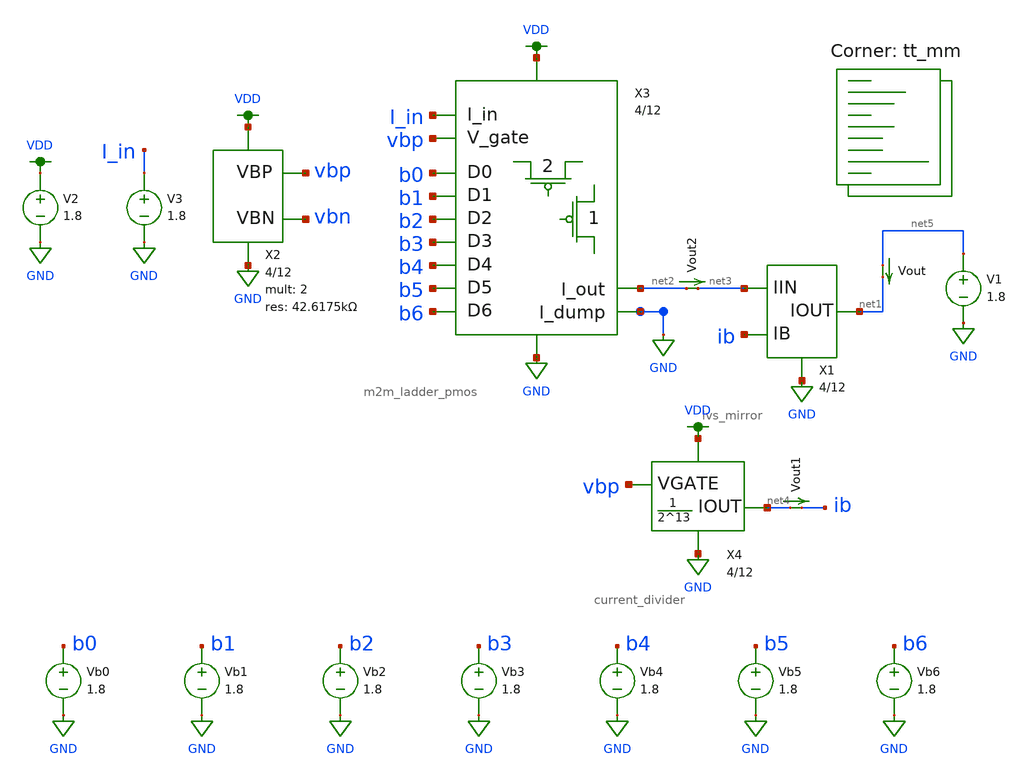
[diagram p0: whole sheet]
** sch_path: dac/schematic/m2m_ladder_biased_mirrored_mm_tb.sch
**.subckt m2m_ladder_biased_mirrored_mm_tb
Vb0 b0 GND 1.8
Vb1 b1 GND 1.8
Vb2 b2 GND 1.8
Vb3 b3 GND 1.8
Vb4 b4 GND 1.8
Vb5 b5 GND 1.8
Vb6 b6 GND 1.8
V2 VDD GND 1.8
X2 vbp VDD GND vbn bias_gen u_w=4 u_l=12 m=2 r=42.6175k
V3 I_in GND 1.8
X3 VDD GND b0 b1 b2 b3 b4 b5 b6 vbp I_in GND net2 m2m_ladder_pmos u_w=4 u_l=12
Vout2 net2 net3 0
.save i(vout2)
X1 GND net3 ib net1 lvs_mirror u_w=4 u_l=12 m=2 r=1M
Vout net5 net1 0
.save i(vout)
V1 net5 GND 1.8
X4 GND VDD net4 vbp current_divider u_w=4 u_l=12
Vout1 net4 ib 0
.save i(vout1)
**** begin user architecture code


.control
  set wr_vecnames
  set wr_singlescale
  let code = 0
  while code < 128
    if code eq 0
      let b0 = 0
    else
      let b0 = (code % 2) * 1.8
    end
    if floor(code / 2) eq 0
      let b1 = 0
    else
      let b1 = (floor(code / 2) % 2) * 1.8
    end
    if floor(code / 4) eq 0
      let b2 = 0
    else
      let b2 = (floor(code / 4) % 2) * 1.8
    end
    if floor(code / 8) eq 0
      let b3 = 0
    else
      let b3 = (floor(code / 8) % 2) * 1.8
    end
    if floor(code / 16) eq 0
      let b4 = 0
    else
      let b4 = (floor(code / 16) % 2) * 1.8
    end
    if floor(code / 32) eq 0
      let b5 = 0
    else
      let b5 = (floor(code / 32) % 2) * 1.8
    end
    if floor(code / 64) eq 0
      let b6 = 0
    else
      let b6 = (floor(code / 64) % 2) * 1.8
    end
    alter vb0 $&b0
    alter vb1 $&b1
    alter vb2 $&b2
    alter vb3 $&b3
    alter vb4 $&b4
    alter vb5 $&b5
    alter vb6 $&b6
    save all
    op
    wrdata
+ ~/documents/git/madvlsi/dac/build/m2m_ladder_biased_mirrored_mm/m2m_ladder_biased_mirrored_mm_tb.txt i(Vout) i(Vout1) i(Vout2) i(V3) v(b0) v(b1) v(b2) v(b3) v(b4) v(b5) v(b6)
    if code eq 0
      set appendwrite
      set wr_vecnames = FALSE
    end
    let code = code + 1
  end
  quit
.endc

.lib $::SKYWATER_MODELS/sky130.lib.spice tt_mm
**** end user architecture code
**.ends
.GLOBAL GND
.GLOBAL VDD
.end
